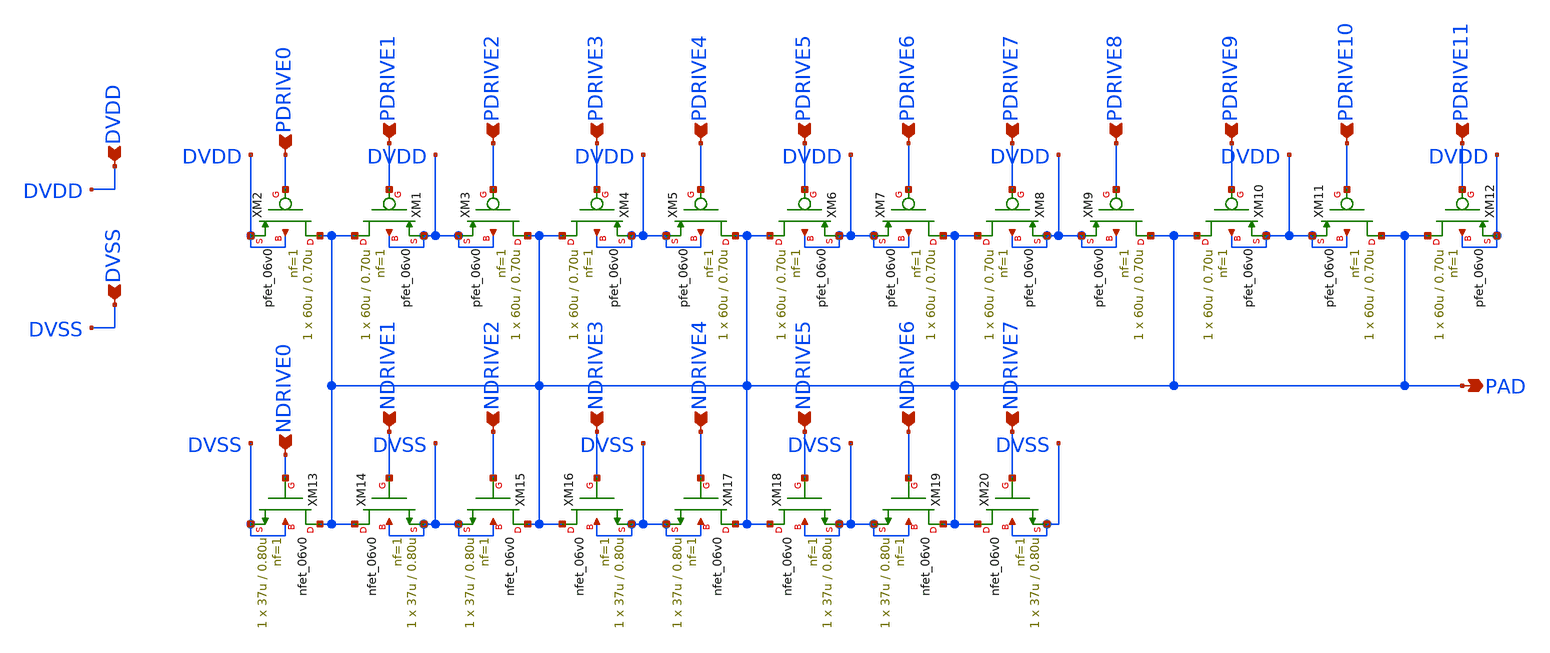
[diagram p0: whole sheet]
** sch_path: gf180mcu_fd_io__bi_24t/comp018green_out_paddrv_24T.sch
**.subckt comp018green_out_paddrv_24T PDRIVE0 PDRIVE1 PDRIVE2 PDRIVE3 PDRIVE4 PDRIVE5 PDRIVE6
*+ PDRIVE7 PDRIVE8 PDRIVE9 PDRIVE10 PDRIVE11 PAD NDRIVE0 NDRIVE1 NDRIVE2 NDRIVE3 NDRIVE4 NDRIVE5 NDRIVE6
*+ NDRIVE7 DVDD DVSS
*.ipin PDRIVE0
*.ipin PDRIVE1
*.ipin PDRIVE2
*.ipin PDRIVE3
*.ipin PDRIVE4
*.ipin PDRIVE5
*.ipin PDRIVE6
*.ipin PDRIVE7
*.ipin PDRIVE8
*.ipin PDRIVE9
*.ipin PDRIVE10
*.ipin PDRIVE11
*.opin PAD
*.ipin NDRIVE0
*.ipin NDRIVE1
*.ipin NDRIVE2
*.ipin NDRIVE3
*.ipin NDRIVE4
*.ipin NDRIVE5
*.ipin NDRIVE6
*.ipin NDRIVE7
*.ipin DVDD
*.ipin DVSS
XM1 PAD PDRIVE1 DVDD DVDD pfet_06v0 L=0.70u W=60u nf=1 ad='int((nf+1)/2) * W/nf * 0.18u' as='int((nf+2)/2) * W/nf * 0.18u'
+ pd='2*int((nf+1)/2) * (W/nf + 0.18u)' ps='2*int((nf+2)/2) * (W/nf + 0.18u)' nrd='0.18u / W' nrs='0.18u / W'
+ sa=0 sb=0 sd=0 m=1
XM2 PAD PDRIVE0 DVDD DVDD pfet_06v0 L=0.70u W=60u nf=1 ad='int((nf+1)/2) * W/nf * 0.18u' as='int((nf+2)/2) * W/nf * 0.18u'
+ pd='2*int((nf+1)/2) * (W/nf + 0.18u)' ps='2*int((nf+2)/2) * (W/nf + 0.18u)' nrd='0.18u / W' nrs='0.18u / W'
+ sa=0 sb=0 sd=0 m=1
XM3 PAD PDRIVE2 DVDD DVDD pfet_06v0 L=0.70u W=60u nf=1 ad='int((nf+1)/2) * W/nf * 0.18u' as='int((nf+2)/2) * W/nf * 0.18u'
+ pd='2*int((nf+1)/2) * (W/nf + 0.18u)' ps='2*int((nf+2)/2) * (W/nf + 0.18u)' nrd='0.18u / W' nrs='0.18u / W'
+ sa=0 sb=0 sd=0 m=1
XM4 PAD PDRIVE3 DVDD DVDD pfet_06v0 L=0.70u W=60u nf=1 ad='int((nf+1)/2) * W/nf * 0.18u' as='int((nf+2)/2) * W/nf * 0.18u'
+ pd='2*int((nf+1)/2) * (W/nf + 0.18u)' ps='2*int((nf+2)/2) * (W/nf + 0.18u)' nrd='0.18u / W' nrs='0.18u / W'
+ sa=0 sb=0 sd=0 m=1
XM5 PAD PDRIVE4 DVDD DVDD pfet_06v0 L=0.70u W=60u nf=1 ad='int((nf+1)/2) * W/nf * 0.18u' as='int((nf+2)/2) * W/nf * 0.18u'
+ pd='2*int((nf+1)/2) * (W/nf + 0.18u)' ps='2*int((nf+2)/2) * (W/nf + 0.18u)' nrd='0.18u / W' nrs='0.18u / W'
+ sa=0 sb=0 sd=0 m=1
XM6 PAD PDRIVE5 DVDD DVDD pfet_06v0 L=0.70u W=60u nf=1 ad='int((nf+1)/2) * W/nf * 0.18u' as='int((nf+2)/2) * W/nf * 0.18u'
+ pd='2*int((nf+1)/2) * (W/nf + 0.18u)' ps='2*int((nf+2)/2) * (W/nf + 0.18u)' nrd='0.18u / W' nrs='0.18u / W'
+ sa=0 sb=0 sd=0 m=1
XM7 PAD PDRIVE6 DVDD DVDD pfet_06v0 L=0.70u W=60u nf=1 ad='int((nf+1)/2) * W/nf * 0.18u' as='int((nf+2)/2) * W/nf * 0.18u'
+ pd='2*int((nf+1)/2) * (W/nf + 0.18u)' ps='2*int((nf+2)/2) * (W/nf + 0.18u)' nrd='0.18u / W' nrs='0.18u / W'
+ sa=0 sb=0 sd=0 m=1
XM8 PAD PDRIVE7 DVDD DVDD pfet_06v0 L=0.70u W=60u nf=1 ad='int((nf+1)/2) * W/nf * 0.18u' as='int((nf+2)/2) * W/nf * 0.18u'
+ pd='2*int((nf+1)/2) * (W/nf + 0.18u)' ps='2*int((nf+2)/2) * (W/nf + 0.18u)' nrd='0.18u / W' nrs='0.18u / W'
+ sa=0 sb=0 sd=0 m=1
XM9 PAD PDRIVE8 DVDD DVDD pfet_06v0 L=0.70u W=60u nf=1 ad='int((nf+1)/2) * W/nf * 0.18u' as='int((nf+2)/2) * W/nf * 0.18u'
+ pd='2*int((nf+1)/2) * (W/nf + 0.18u)' ps='2*int((nf+2)/2) * (W/nf + 0.18u)' nrd='0.18u / W' nrs='0.18u / W'
+ sa=0 sb=0 sd=0 m=1
XM10 PAD PDRIVE9 DVDD DVDD pfet_06v0 L=0.70u W=60u nf=1 ad='int((nf+1)/2) * W/nf * 0.18u' as='int((nf+2)/2) * W/nf * 0.18u'
+ pd='2*int((nf+1)/2) * (W/nf + 0.18u)' ps='2*int((nf+2)/2) * (W/nf + 0.18u)' nrd='0.18u / W' nrs='0.18u / W'
+ sa=0 sb=0 sd=0 m=1
XM11 PAD PDRIVE10 DVDD DVDD pfet_06v0 L=0.70u W=60u nf=1 ad='int((nf+1)/2) * W/nf * 0.18u' as='int((nf+2)/2) * W/nf * 0.18u'
+ pd='2*int((nf+1)/2) * (W/nf + 0.18u)' ps='2*int((nf+2)/2) * (W/nf + 0.18u)' nrd='0.18u / W' nrs='0.18u / W'
+ sa=0 sb=0 sd=0 m=1
XM12 PAD PDRIVE11 DVDD DVDD pfet_06v0 L=0.70u W=60u nf=1 ad='int((nf+1)/2) * W/nf * 0.18u' as='int((nf+2)/2) * W/nf * 0.18u'
+ pd='2*int((nf+1)/2) * (W/nf + 0.18u)' ps='2*int((nf+2)/2) * (W/nf + 0.18u)' nrd='0.18u / W' nrs='0.18u / W'
+ sa=0 sb=0 sd=0 m=1
XM13 PAD NDRIVE0 DVSS DVSS nfet_06v0 L=0.80u W=37u nf=1 ad='int((nf+1)/2) * W/nf * 0.18u' as='int((nf+2)/2) * W/nf * 0.18u'
+ pd='2*int((nf+1)/2) * (W/nf + 0.18u)' ps='2*int((nf+2)/2) * (W/nf + 0.18u)' nrd='0.18u / W' nrs='0.18u / W'
+ sa=0 sb=0 sd=0 m=1
XM14 PAD NDRIVE1 DVSS DVSS nfet_06v0 L=0.80u W=37u nf=1 ad='int((nf+1)/2) * W/nf * 0.18u' as='int((nf+2)/2) * W/nf * 0.18u'
+ pd='2*int((nf+1)/2) * (W/nf + 0.18u)' ps='2*int((nf+2)/2) * (W/nf + 0.18u)' nrd='0.18u / W' nrs='0.18u / W'
+ sa=0 sb=0 sd=0 m=1
XM15 PAD NDRIVE2 DVSS DVSS nfet_06v0 L=0.80u W=37u nf=1 ad='int((nf+1)/2) * W/nf * 0.18u' as='int((nf+2)/2) * W/nf * 0.18u'
+ pd='2*int((nf+1)/2) * (W/nf + 0.18u)' ps='2*int((nf+2)/2) * (W/nf + 0.18u)' nrd='0.18u / W' nrs='0.18u / W'
+ sa=0 sb=0 sd=0 m=1
XM16 PAD NDRIVE3 DVSS DVSS nfet_06v0 L=0.80u W=37u nf=1 ad='int((nf+1)/2) * W/nf * 0.18u' as='int((nf+2)/2) * W/nf * 0.18u'
+ pd='2*int((nf+1)/2) * (W/nf + 0.18u)' ps='2*int((nf+2)/2) * (W/nf + 0.18u)' nrd='0.18u / W' nrs='0.18u / W'
+ sa=0 sb=0 sd=0 m=1
XM17 PAD NDRIVE4 DVSS DVSS nfet_06v0 L=0.80u W=37u nf=1 ad='int((nf+1)/2) * W/nf * 0.18u' as='int((nf+2)/2) * W/nf * 0.18u'
+ pd='2*int((nf+1)/2) * (W/nf + 0.18u)' ps='2*int((nf+2)/2) * (W/nf + 0.18u)' nrd='0.18u / W' nrs='0.18u / W'
+ sa=0 sb=0 sd=0 m=1
XM18 PAD NDRIVE5 DVSS DVSS nfet_06v0 L=0.80u W=37u nf=1 ad='int((nf+1)/2) * W/nf * 0.18u' as='int((nf+2)/2) * W/nf * 0.18u'
+ pd='2*int((nf+1)/2) * (W/nf + 0.18u)' ps='2*int((nf+2)/2) * (W/nf + 0.18u)' nrd='0.18u / W' nrs='0.18u / W'
+ sa=0 sb=0 sd=0 m=1
XM19 PAD NDRIVE6 DVSS DVSS nfet_06v0 L=0.80u W=37u nf=1 ad='int((nf+1)/2) * W/nf * 0.18u' as='int((nf+2)/2) * W/nf * 0.18u'
+ pd='2*int((nf+1)/2) * (W/nf + 0.18u)' ps='2*int((nf+2)/2) * (W/nf + 0.18u)' nrd='0.18u / W' nrs='0.18u / W'
+ sa=0 sb=0 sd=0 m=1
XM20 PAD NDRIVE7 DVSS DVSS nfet_06v0 L=0.80u W=37u nf=1 ad='int((nf+1)/2) * W/nf * 0.18u' as='int((nf+2)/2) * W/nf * 0.18u'
+ pd='2*int((nf+1)/2) * (W/nf + 0.18u)' ps='2*int((nf+2)/2) * (W/nf + 0.18u)' nrd='0.18u / W' nrs='0.18u / W'
+ sa=0 sb=0 sd=0 m=1
**.ends
.end
